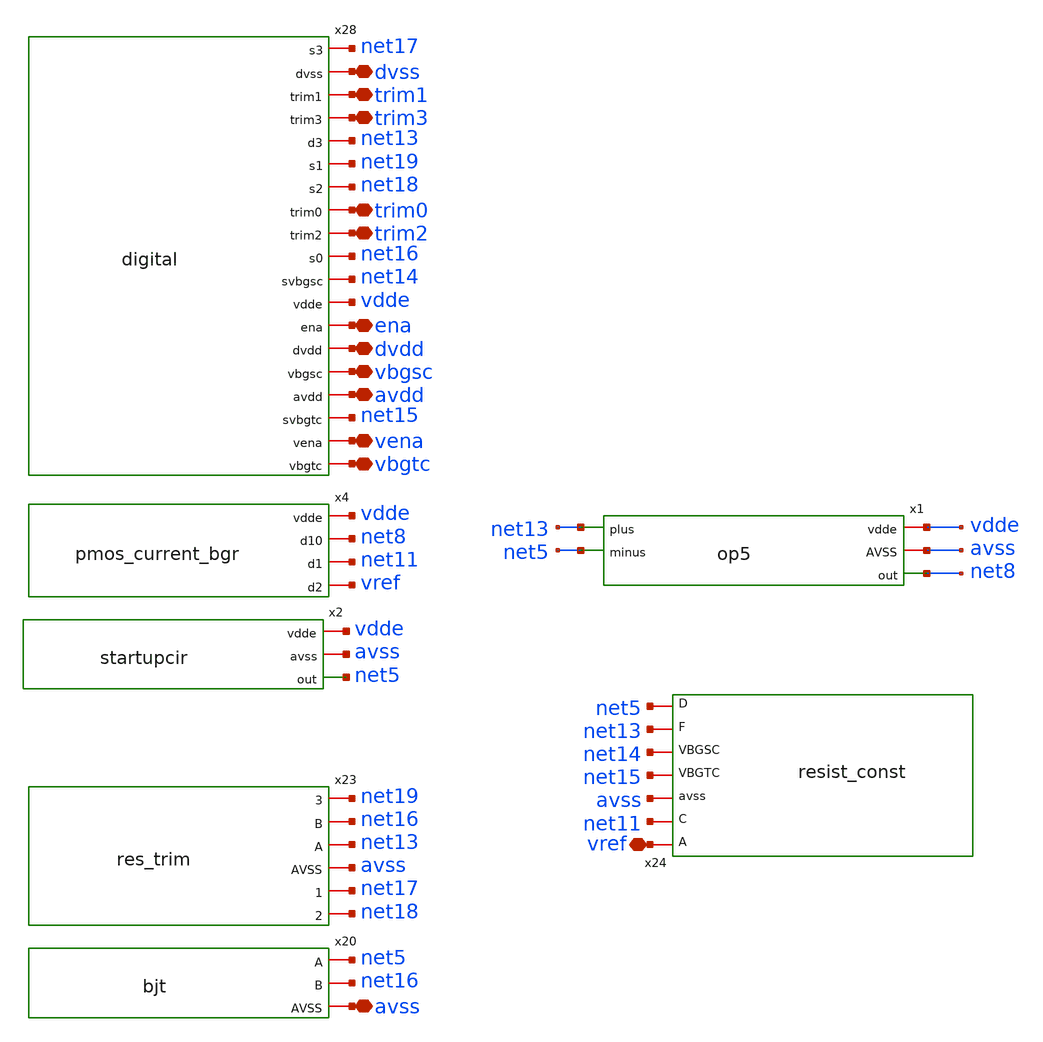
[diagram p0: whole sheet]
** sch_path: magic/bgr_op5_block_rev1.sch
**.subckt bgr_op5_block_rev1 trim1 trim3 trim0 trim2 dvdd vbgsc vbgtc avdd vena ena avss dvss vref
*.iopin trim1
*.iopin trim3
*.iopin trim0
*.iopin trim2
*.iopin dvdd
*.iopin vbgsc
*.iopin vbgtc
*.iopin avdd
*.iopin vena
*.iopin ena
*.iopin avss
*.iopin dvss
*.iopin vref
x4 vdde net8 net11 vref pmos_current_bgr
x20 net5 net16 avss bjt
x23 net19 net16 net13 avss net17 net18 res_trim
x24 vref net11 avss net15 net14 net13 net5 resist_const
x28 net17 dvss trim1 trim3 net13 net19 net18 trim0 trim2 net16 net14 vdde ena dvdd vbgsc avdd net15
+ vena vbgtc digital
x1 vdde avss net13 net5 net8 op5
x2 vdde avss net5 startupcir
**.ends
.end
